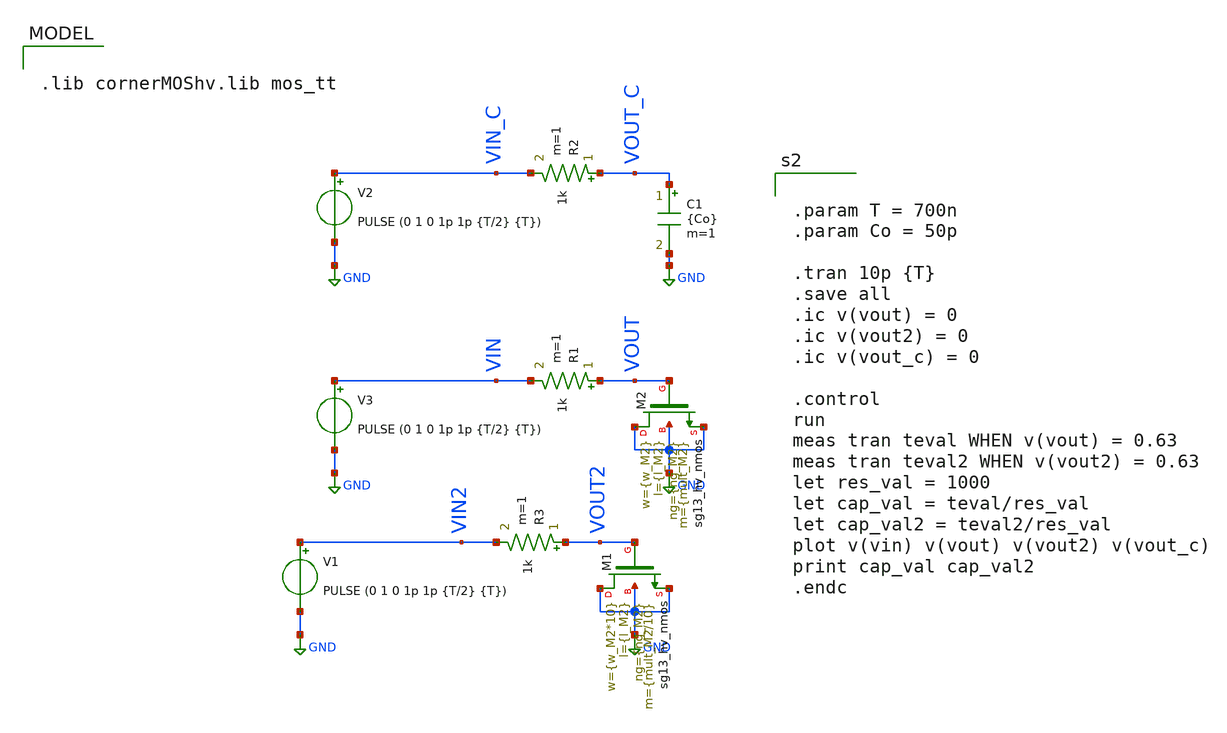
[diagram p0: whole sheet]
** sch_path: xschem/DCDCBuck/TB_powerNMOS_cgate_ext.sch
**.subckt TB_powerNMOS_cgate_ext
R1 VOUT VIN 1k m=1
XM2 GND VOUT GND GND sg13_hv_nmos w={w_M2} l={l_M2} ng={ng_M2} m={mult_M2} mm_ok=1
R2 VOUT_C VIN_C 1k m=1
V2 VIN_C GND PULSE (0 1 0 1p 1p {T/2} {T})
C1 VOUT_C GND {Co} m=1
V3 VIN GND PULSE (0 1 0 1p 1p {T/2} {T})
R3 VOUT2 VIN2 1k m=1
XM1 GND VOUT2 GND GND sg13_hv_nmos w={w_M2*10} l={l_M2} ng={ng_M2} m={mult_M2/10} mm_ok=1
V1 VIN2 GND PULSE (0 1 0 1p 1p {T/2} {T})
**** begin user architecture code

.lib cornerMOShv.lib mos_tt



.param T = 700n
.param Co = 50p

.tran 10p {T}
.save all
.ic v(vout) = 0
.ic v(vout2) = 0
.ic v(vout_c) = 0

.control
run
meas tran teval WHEN v(vout) = 0.63
meas tran teval2 WHEN v(vout2) = 0.63
let res_val = 1000
let cap_val = teval/res_val
let cap_val2 = teval2/res_val
plot v(vin) v(vout) v(vout2) v(vout_c)
print cap_val cap_val2
.endc




.param mult = 95238
.param temp=27
.param mult_M1 = 3*mult
.param w_M1 =0.3u
.param l_M1 = 0.45u
.param ng_M1 = 1

.param mult_M2 = 1*mult
.param w_M2 =0.3u
.param l_M2 =0.45u
.param ng_M2 =1





**** end user architecture code
**.ends
.GLOBAL GND
.end
